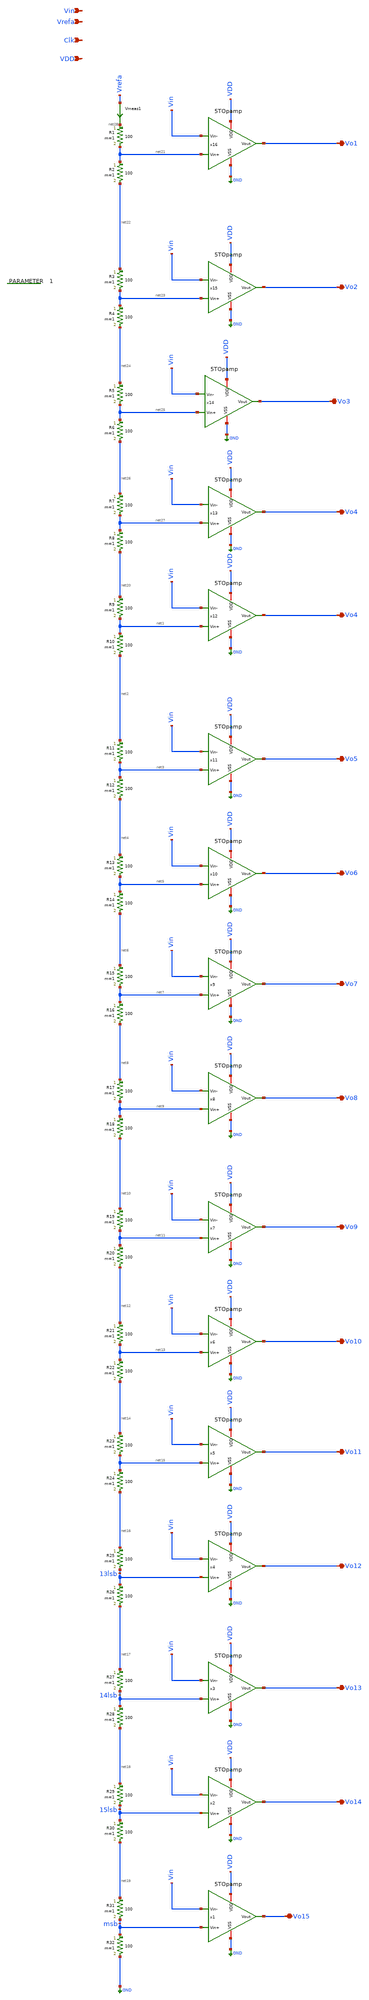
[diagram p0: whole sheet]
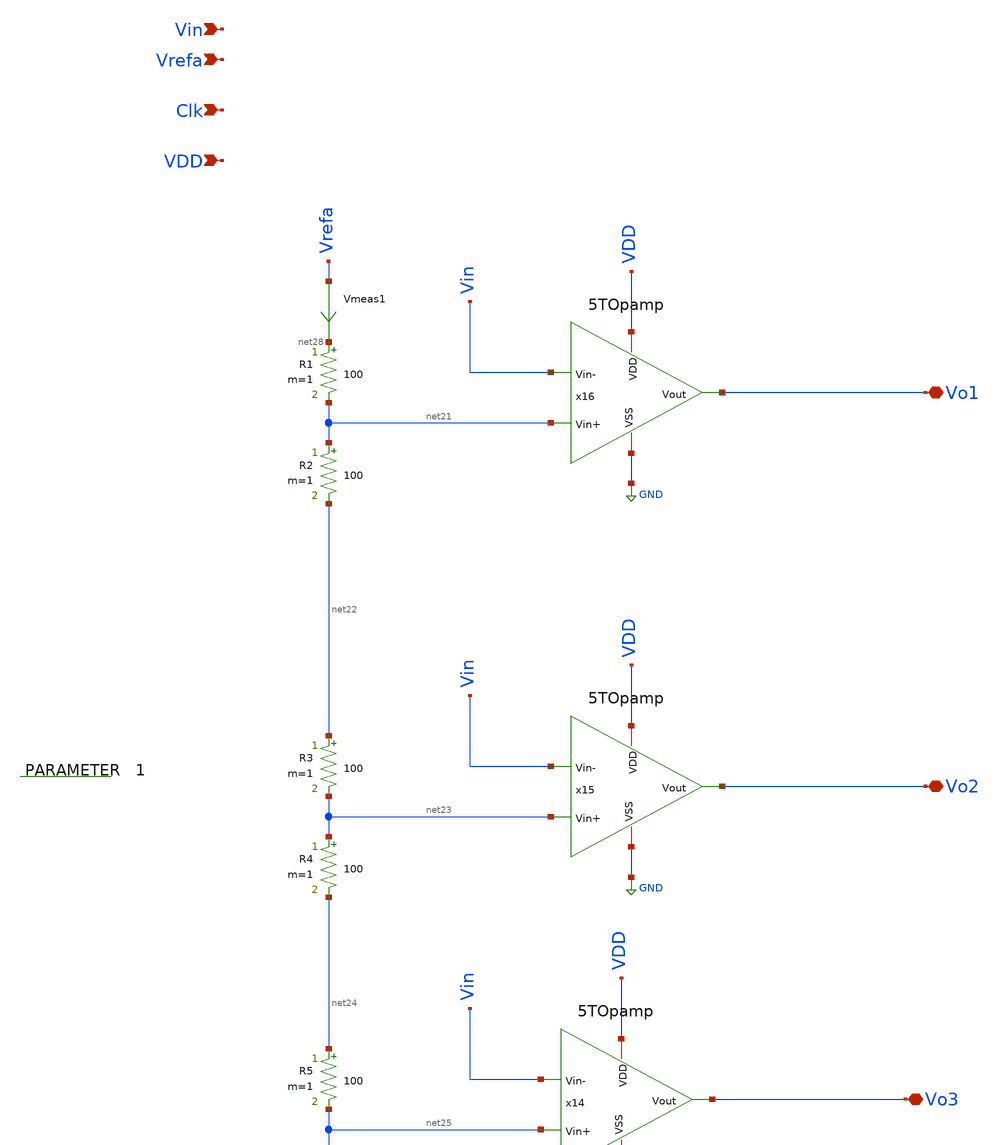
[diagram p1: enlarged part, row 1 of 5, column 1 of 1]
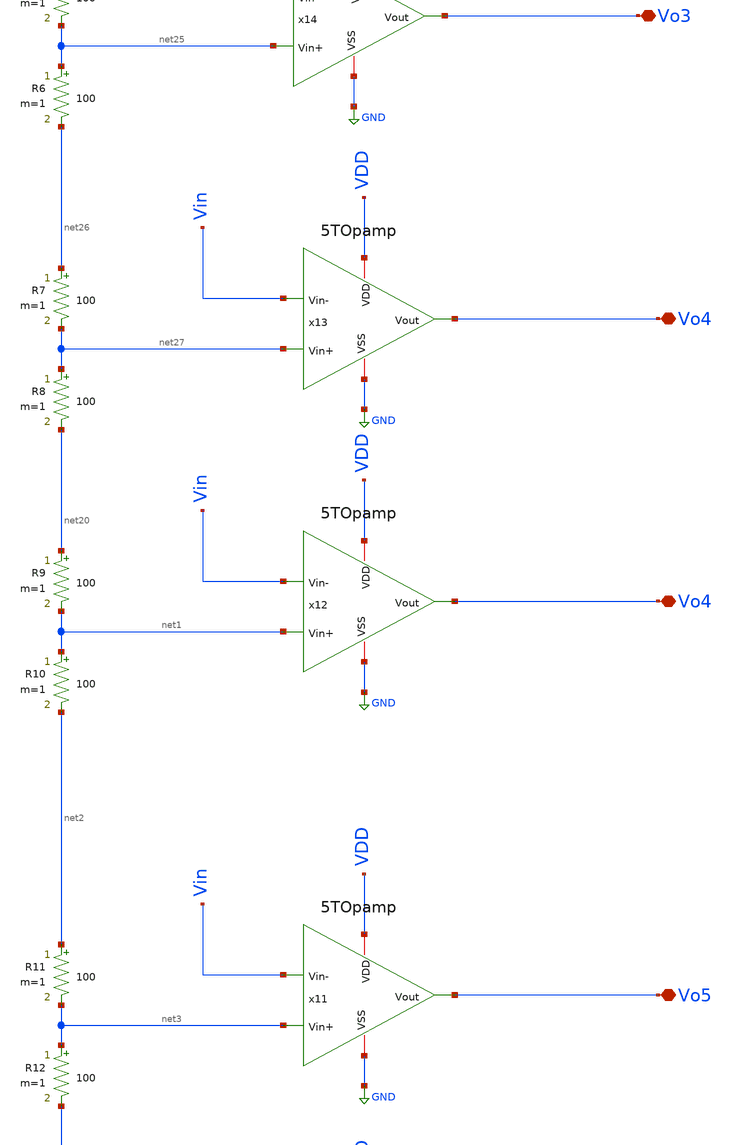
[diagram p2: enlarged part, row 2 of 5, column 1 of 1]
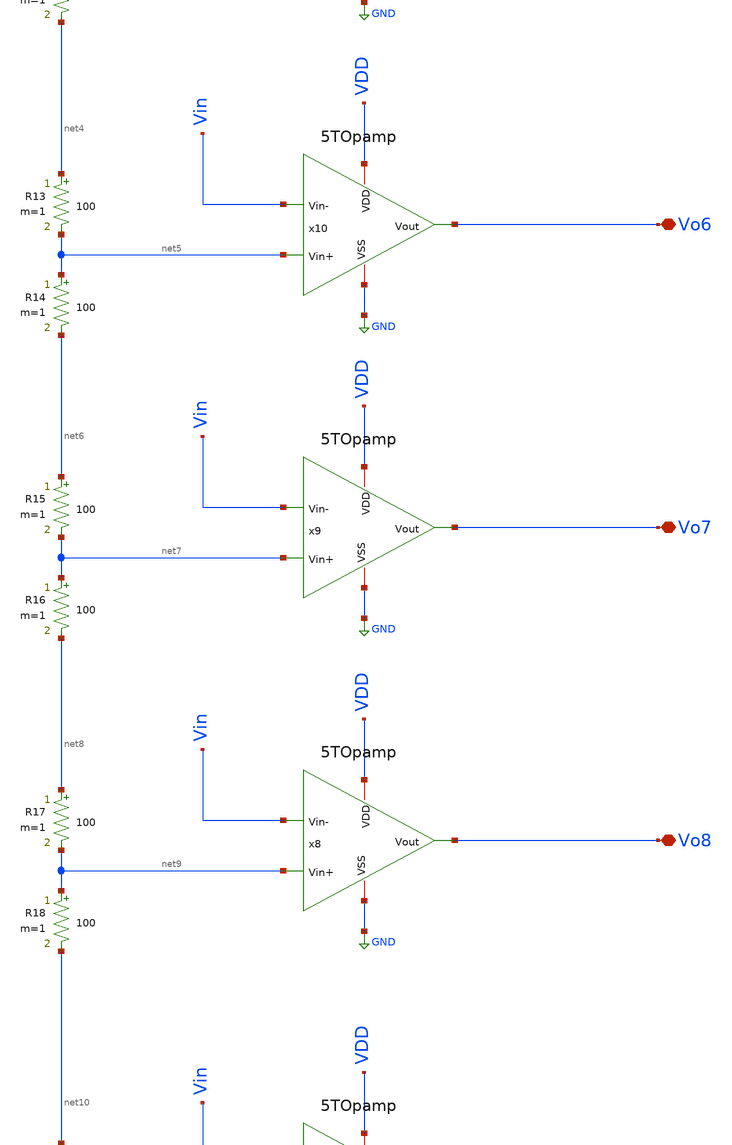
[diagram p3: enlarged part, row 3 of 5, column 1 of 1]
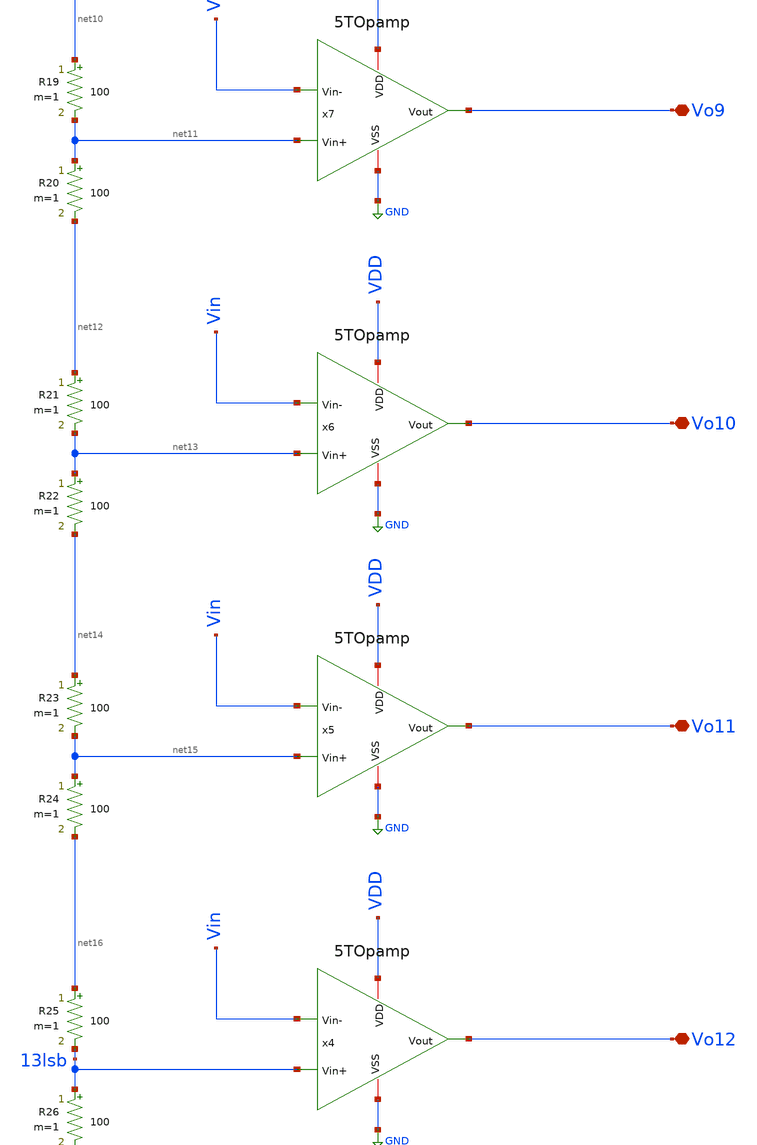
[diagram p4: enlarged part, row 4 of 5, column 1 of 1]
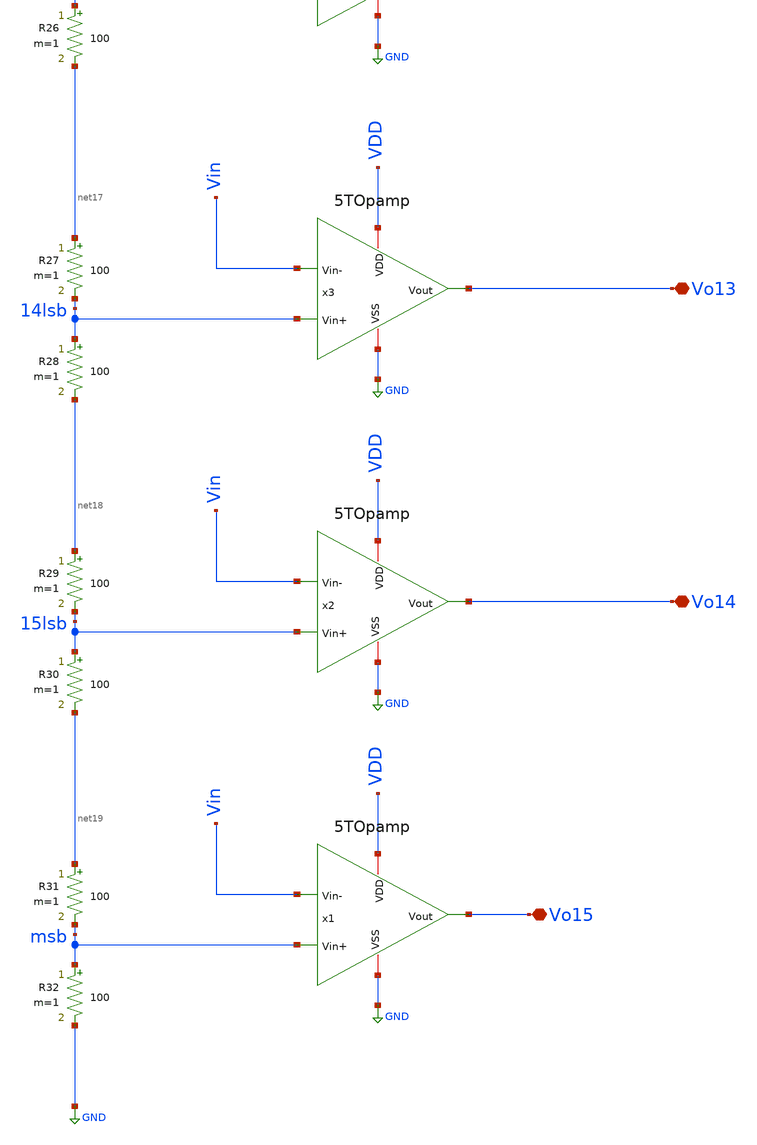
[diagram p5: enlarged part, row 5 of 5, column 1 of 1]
** sch_path: xschem/DataConverters/4bitADCwop.sch
**.subckt 4bitADCwop Vin Vrefa Clk VDD Vo1 Vo2 Vo3 Vo4 Vo4 Vo5 Vo6 Vo7 Vo8 Vo9 Vo10 Vo11 Vo12 Vo13
*+ Vo14 Vo15
*.ipin Vin
*.ipin Vrefa
*.ipin Clk
*.ipin VDD
*.iopin Vo1
*.iopin Vo2
*.iopin Vo3
*.iopin Vo4
*.iopin Vo4
*.iopin Vo5
*.iopin Vo6
*.iopin Vo7
*.iopin Vo8
*.iopin Vo9
*.iopin Vo10
*.iopin Vo11
*.iopin Vo12
*.iopin Vo13
*.iopin Vo14
*.iopin Vo15
Vmeas1 Vrefa net28 0
.save i(vmeas1)
R1 net28 net21 100 m=1
R2 net21 net22 100 m=1
R3 net22 net23 100 m=1
R4 net23 net24 100 m=1
R5 net24 net25 100 m=1
R6 net25 net26 100 m=1
R7 net26 net27 100 m=1
R8 net27 net20 100 m=1
R9 net20 net1 100 m=1
R10 net1 net2 100 m=1
R11 net2 net3 100 m=1
R12 net3 net4 100 m=1
R13 net4 net5 100 m=1
R14 net5 net6 100 m=1
R15 net6 net7 100 m=1
R16 net7 net8 100 m=1
R17 net8 net9 100 m=1
R18 net9 net10 100 m=1
R19 net10 net11 100 m=1
R20 net11 net12 100 m=1
R21 net12 net13 100 m=1
R22 net13 net14 100 m=1
R23 net14 net15 100 m=1
R24 net15 net16 100 m=1
R25 net16 13lsb 100 m=1
R26 13lsb net17 100 m=1
R27 net17 14lsb 100 m=1
R28 14lsb net18 100 m=1
R29 net18 15lsb 100 m=1
R30 15lsb net19 100 m=1
R31 net19 msb 100 m=1
R32 msb GND 100 m=1
.param 1
x1 VDD Vo15 Vin msb GND 5TOpamp
x2 VDD Vo14 Vin 15lsb GND 5TOpamp
x3 VDD Vo13 Vin 14lsb GND 5TOpamp
x4 VDD Vo12 Vin 13lsb GND 5TOpamp
x5 VDD Vo11 Vin net15 GND 5TOpamp
x6 VDD Vo10 Vin net13 GND 5TOpamp
x7 VDD Vo9 Vin net11 GND 5TOpamp
x8 VDD Vo8 Vin net9 GND 5TOpamp
x9 VDD Vo7 Vin net7 GND 5TOpamp
x10 VDD Vo6 Vin net5 GND 5TOpamp
x11 VDD Vo5 Vin net3 GND 5TOpamp
x12 VDD Vo4 Vin net1 GND 5TOpamp
x13 VDD Vo4 Vin net27 GND 5TOpamp
x14 VDD Vo3 Vin net25 GND 5TOpamp
x15 VDD Vo2 Vin net23 GND 5TOpamp
x16 VDD Vo1 Vin net21 GND 5TOpamp
**.ends

* expanding   symbol:  Amplifiers/5TOpamp.sym # of pins=5
** sym_path: xschem/Amplifiers/5TOpamp.sym
** sch_path: xschem/Amplifiers/5TOpamp.sch
.subckt 5TOpamp VDD Vout Vin- Vin+ VSS
*.iopin VDD
*.iopin VSS
*.ipin Vin-
*.ipin Vin+
*.opin Vout
I0 VDD Vb1 50u
XM1 Vcm Vin+ Vsink VSS sky130_fd_pr__nfet_01v8 L=0.75 W=4 nf=1 ad='int((nf+1)/2) * W/nf * 0.29' as='int((nf+2)/2) * W/nf * 0.29'
+ pd='2*int((nf+1)/2) * (W/nf + 0.29)' ps='2*int((nf+2)/2) * (W/nf + 0.29)' nrd='0.29 / W' nrs='0.29 / W'
+ sa=0 sb=0 sd=0 mult=3 m=3
XM2 Vout Vin- Vsink VSS sky130_fd_pr__nfet_01v8 L=0.75 W=4 nf=1 ad='int((nf+1)/2) * W/nf * 0.29' as='int((nf+2)/2) * W/nf * 0.29'
+ pd='2*int((nf+1)/2) * (W/nf + 0.29)' ps='2*int((nf+2)/2) * (W/nf + 0.29)' nrd='0.29 / W' nrs='0.29 / W'
+ sa=0 sb=0 sd=0 mult=3 m=3
XM3 Vb1 Vb1 VSS VSS sky130_fd_pr__nfet_01v8 L=0.75 W=5 nf=1 ad='int((nf+1)/2) * W/nf * 0.29' as='int((nf+2)/2) * W/nf * 0.29'
+ pd='2*int((nf+1)/2) * (W/nf + 0.29)' ps='2*int((nf+2)/2) * (W/nf + 0.29)' nrd='0.29 / W' nrs='0.29 / W'
+ sa=0 sb=0 sd=0 mult=1 m=1
XM4 Vsink Vb1 VSS VSS sky130_fd_pr__nfet_01v8 L=0.75 W=5 nf=1 ad='int((nf+1)/2) * W/nf * 0.29' as='int((nf+2)/2) * W/nf * 0.29'
+ pd='2*int((nf+1)/2) * (W/nf + 0.29)' ps='2*int((nf+2)/2) * (W/nf + 0.29)' nrd='0.29 / W' nrs='0.29 / W'
+ sa=0 sb=0 sd=0 mult=4 m=4
XM5 Vcm Vcm VDD VDD sky130_fd_pr__pfet_01v8_lvt L=0.75 W=10 nf=1 ad='int((nf+1)/2) * W/nf * 0.29' as='int((nf+2)/2) * W/nf * 0.29'
+ pd='2*int((nf+1)/2) * (W/nf + 0.29)' ps='2*int((nf+2)/2) * (W/nf + 0.29)' nrd='0.29 / W' nrs='0.29 / W'
+ sa=0 sb=0 sd=0 mult=1 m=1
XM6 Vout Vcm VDD VDD sky130_fd_pr__pfet_01v8_lvt L=0.75 W=10 nf=1 ad='int((nf+1)/2) * W/nf * 0.29' as='int((nf+2)/2) * W/nf * 0.29'
+ pd='2*int((nf+1)/2) * (W/nf + 0.29)' ps='2*int((nf+2)/2) * (W/nf + 0.29)' nrd='0.29 / W' nrs='0.29 / W'
+ sa=0 sb=0 sd=0 mult=1 m=1
.ends

.GLOBAL GND
.end
